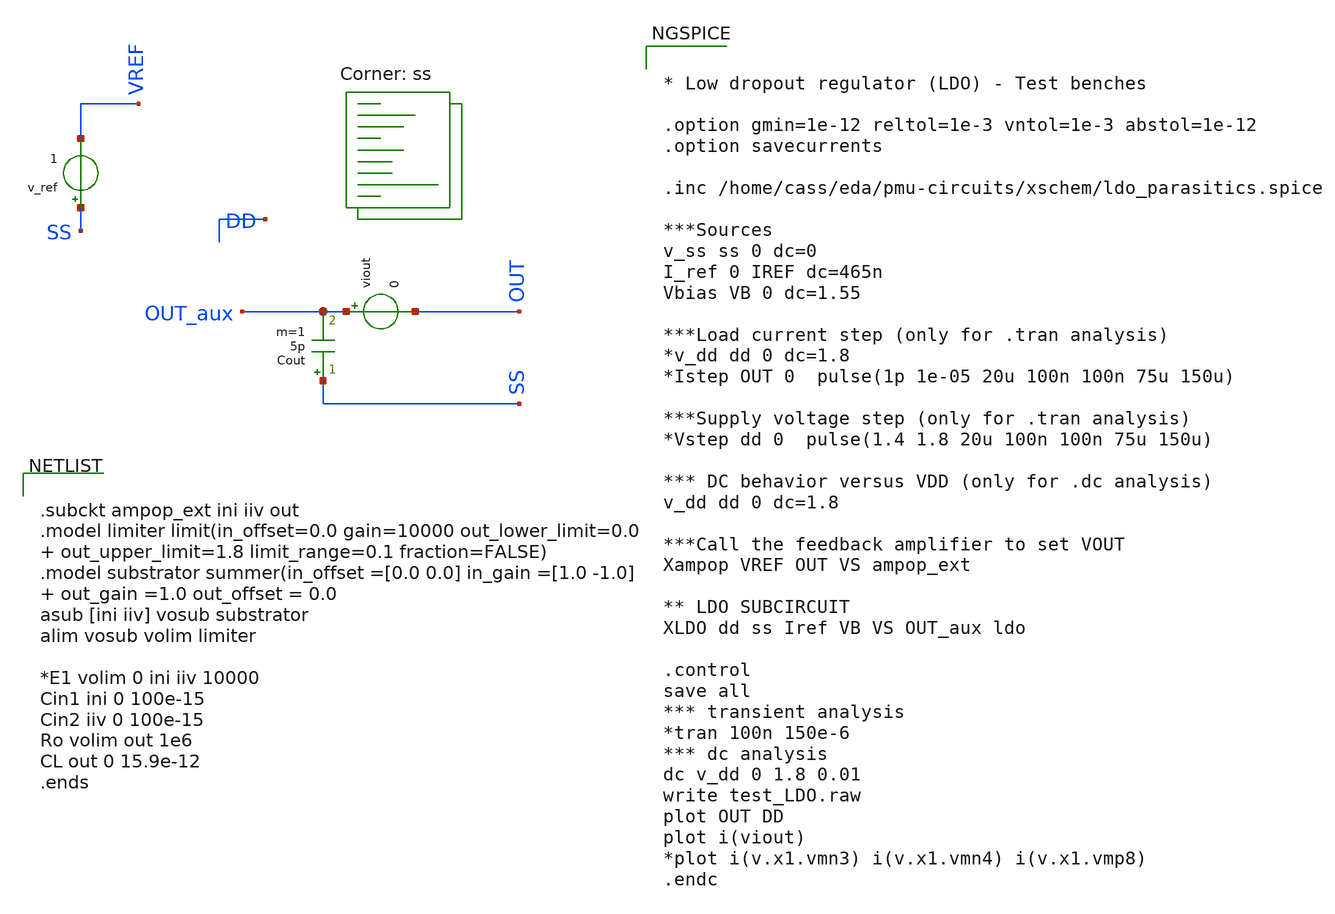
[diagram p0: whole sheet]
** sch_path: xschem/test_ldo_extracted.sch
**.subckt test_ldo_extracted
Cout SS OUT_aux 5p m=1
viout OUT_aux OUT 0
v_ref SS VREF 1
**** begin user architecture code
.lib $::SKYWATER_MODELS/sky130.lib.spice ss


* Low dropout regulator (LDO) - Test benches

.option gmin=1e-12 reltol=1e-3 vntol=1e-3 abstol=1e-12
.option savecurrents

.inc /home/cass/eda/pmu-circuits/xschem/ldo_parasitics.spice

***Sources
v_ss ss 0 dc=0
I_ref 0 IREF dc=465n
Vbias VB 0 dc=1.55

***Load current step (only for .tran analysis)
*v_dd dd 0 dc=1.8
*Istep OUT 0  pulse(1p 1e-05 20u 100n 100n 75u 150u)

***Supply voltage step (only for .tran analysis)
*Vstep dd 0  pulse(1.4 1.8 20u 100n 100n 75u 150u)

*** DC behavior versus VDD (only for .dc analysis)
v_dd dd 0 dc=1.8

***Call the feedback amplifier to set VOUT
Xampop VREF OUT VS ampop_ext

** LDO SUBCIRCUIT
XLDO dd ss Iref VB VS OUT_aux ldo

.control
save all
*** transient analysis
*tran 100n 150e-6
*** dc analysis
dc v_dd 0 1.8 0.01
write test_LDO.raw
plot OUT DD
plot i(viout)
*plot i(v.x1.vmn3) i(v.x1.vmn4) i(v.x1.vmp8)
.endc




.subckt ampop_ext ini iiv out
.model limiter limit(in_offset=0.0 gain=10000 out_lower_limit=0.0  out_upper_limit=1.8
+ limit_range=0.1 fraction=FALSE)
.model substrator summer(in_offset =[0.0 0.0] in_gain =[1.0 -1.0]  out_gain =1.0 out_offset = 0.0
asub [ini iiv] vosub substrator
alim vosub volim limiter

*E1 volim 0 ini iiv 10000
Cin1 ini 0 100e-15
Cin2 iiv 0 100e-15
Ro volim out 1e6
CL out 0 15.9e-12
.ends


**** end user architecture code
**.ends
.end
